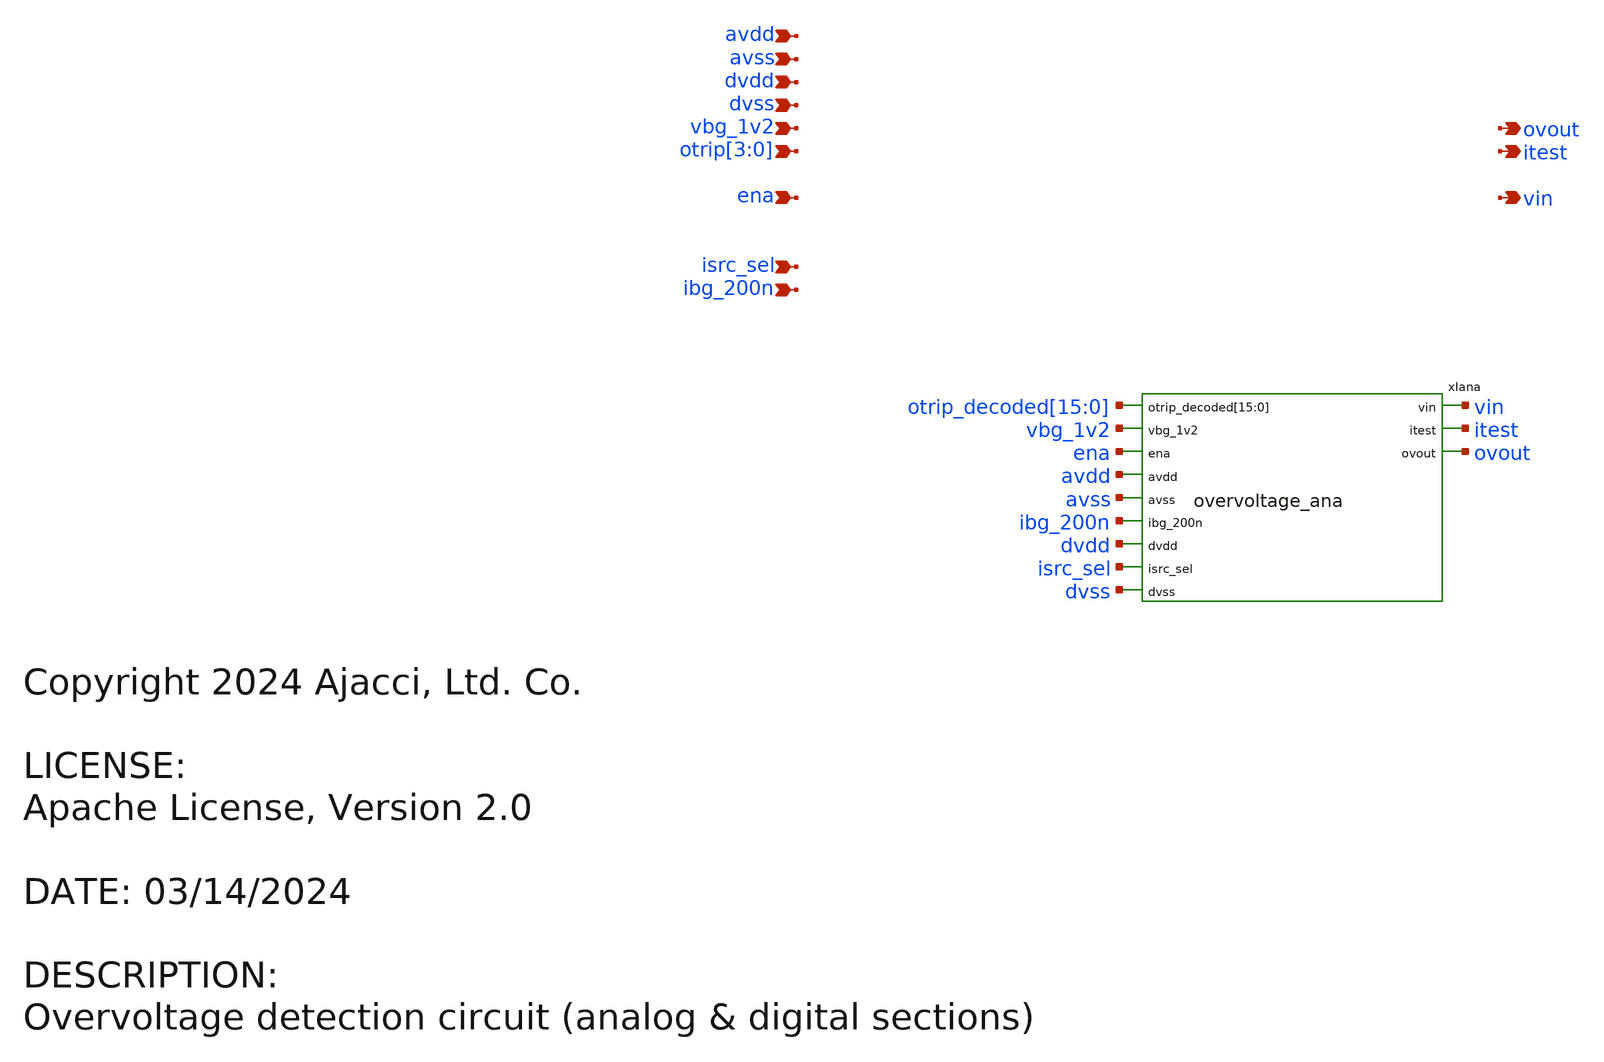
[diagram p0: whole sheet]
** sch_path: xschem/overvoltage.sch
* Copyright 2024 Ajacci, Ltd. Co.
* LICENSE:
* Apache License, Version 2.0
**.subckt overvoltage avdd avss dvdd dvss vbg_1v2 otrip[3],otrip[2],otrip[1],otrip[0] ena isrc_sel
*+ ibg_200n vin ovout itest
*.ipin avdd
*.ipin avss
*.ipin dvdd
*.ipin dvss
*.ipin vbg_1v2
*.ipin otrip[3],otrip[2],otrip[1],otrip[0]
*.ipin ena
*.ipin isrc_sel
*.ipin ibg_200n
*.opin vin
*.opin ovout
*.opin itest
xIana otrip_decoded[15] otrip_decoded[14] otrip_decoded[13] otrip_decoded[12] otrip_decoded[11]
+ otrip_decoded[10] otrip_decoded[9] otrip_decoded[8] otrip_decoded[7] otrip_decoded[6] otrip_decoded[5]
+ otrip_decoded[4] otrip_decoded[3] otrip_decoded[2] otrip_decoded[1] otrip_decoded[0] vin vbg_1v2 ena avdd itest avss
+ ibg_200n dvdd isrc_sel dvss ovout overvoltage_ana
**** begin user architecture code



*XSPICE CO-SIM netlist
.include overvoltage_dig.out.spice
xiovervoltage_dig dvss dvdd  otrip_0_ otrip_1_ otrip_2_ otrip_3_ otrip_decoded_0_  otrip_decoded_10_
+ otrip_decoded_11_ otrip_decoded_12_ otrip_decoded_13_ otrip_decoded_14_ otrip_decoded_15_ otrip_decoded_1_
+ otrip_decoded_2_ otrip_decoded_3_ otrip_decoded_4_ otrip_decoded_5_ otrip_decoded_6_ otrip_decoded_7_
+ otrip_decoded_8_ otrip_decoded_9_  overvoltage_dig


**** end user architecture code
**.ends
.end
